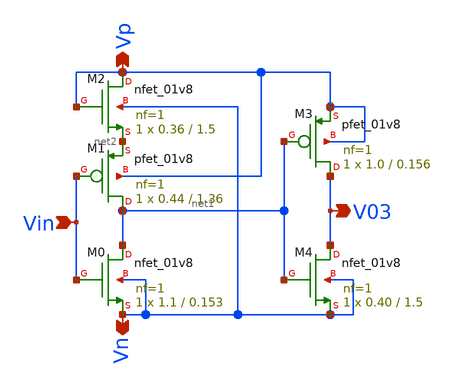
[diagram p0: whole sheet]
** sch_path: xschem/Vth_sch/Symbol/th03.sch
**.subckt th03 Vn Vp Vin V03
*.opin Vn
*.opin Vp
*.ipin Vin
*.opin V03
XM3 V03 net1 Vp Vp sky130_fd_pr__pfet_01v8 L=0.156 W=1.0 nf=1 ad='int((nf+1)/2) * W/nf * 0.29' as='int((nf+2)/2) * W/nf * 0.29'
+ pd='2*int((nf+1)/2) * (W/nf + 0.29)' ps='2*int((nf+2)/2) * (W/nf + 0.29)' nrd='0.29 / W' nrs='0.29 / W'
+ sa=0 sb=0 sd=0 mult=1 m=1
XM4 V03 net1 Vn Vn sky130_fd_pr__nfet_01v8 L=1.5 W=0.40 nf=1 ad='int((nf+1)/2) * W/nf * 0.29' as='int((nf+2)/2) * W/nf * 0.29'
+ pd='2*int((nf+1)/2) * (W/nf + 0.29)' ps='2*int((nf+2)/2) * (W/nf + 0.29)' nrd='0.29 / W' nrs='0.29 / W'
+ sa=0 sb=0 sd=0 mult=1 m=1
XM1 net1 Vin net2 Vp sky130_fd_pr__pfet_01v8 L=1.36 W=0.44 nf=1 ad='int((nf+1)/2) * W/nf * 0.29' as='int((nf+2)/2) * W/nf * 0.29'
+ pd='2*int((nf+1)/2) * (W/nf + 0.29)' ps='2*int((nf+2)/2) * (W/nf + 0.29)' nrd='0.29 / W' nrs='0.29 / W'
+ sa=0 sb=0 sd=0 mult=1 m=1
XM0 net1 Vin Vn Vn sky130_fd_pr__nfet_01v8 L=0.153 W=1.1 nf=1 ad='int((nf+1)/2) * W/nf * 0.29' as='int((nf+2)/2) * W/nf * 0.29'
+ pd='2*int((nf+1)/2) * (W/nf + 0.29)' ps='2*int((nf+2)/2) * (W/nf + 0.29)' nrd='0.29 / W' nrs='0.29 / W'
+ sa=0 sb=0 sd=0 mult=1 m=1
XM2 Vp Vp net2 Vn sky130_fd_pr__nfet_01v8 L=1.5 W=0.36 nf=1 ad='int((nf+1)/2) * W/nf * 0.29' as='int((nf+2)/2) * W/nf * 0.29'
+ pd='2*int((nf+1)/2) * (W/nf + 0.29)' ps='2*int((nf+2)/2) * (W/nf + 0.29)' nrd='0.29 / W' nrs='0.29 / W'
+ sa=0 sb=0 sd=0 mult=1 m=1
**.ends
.end
